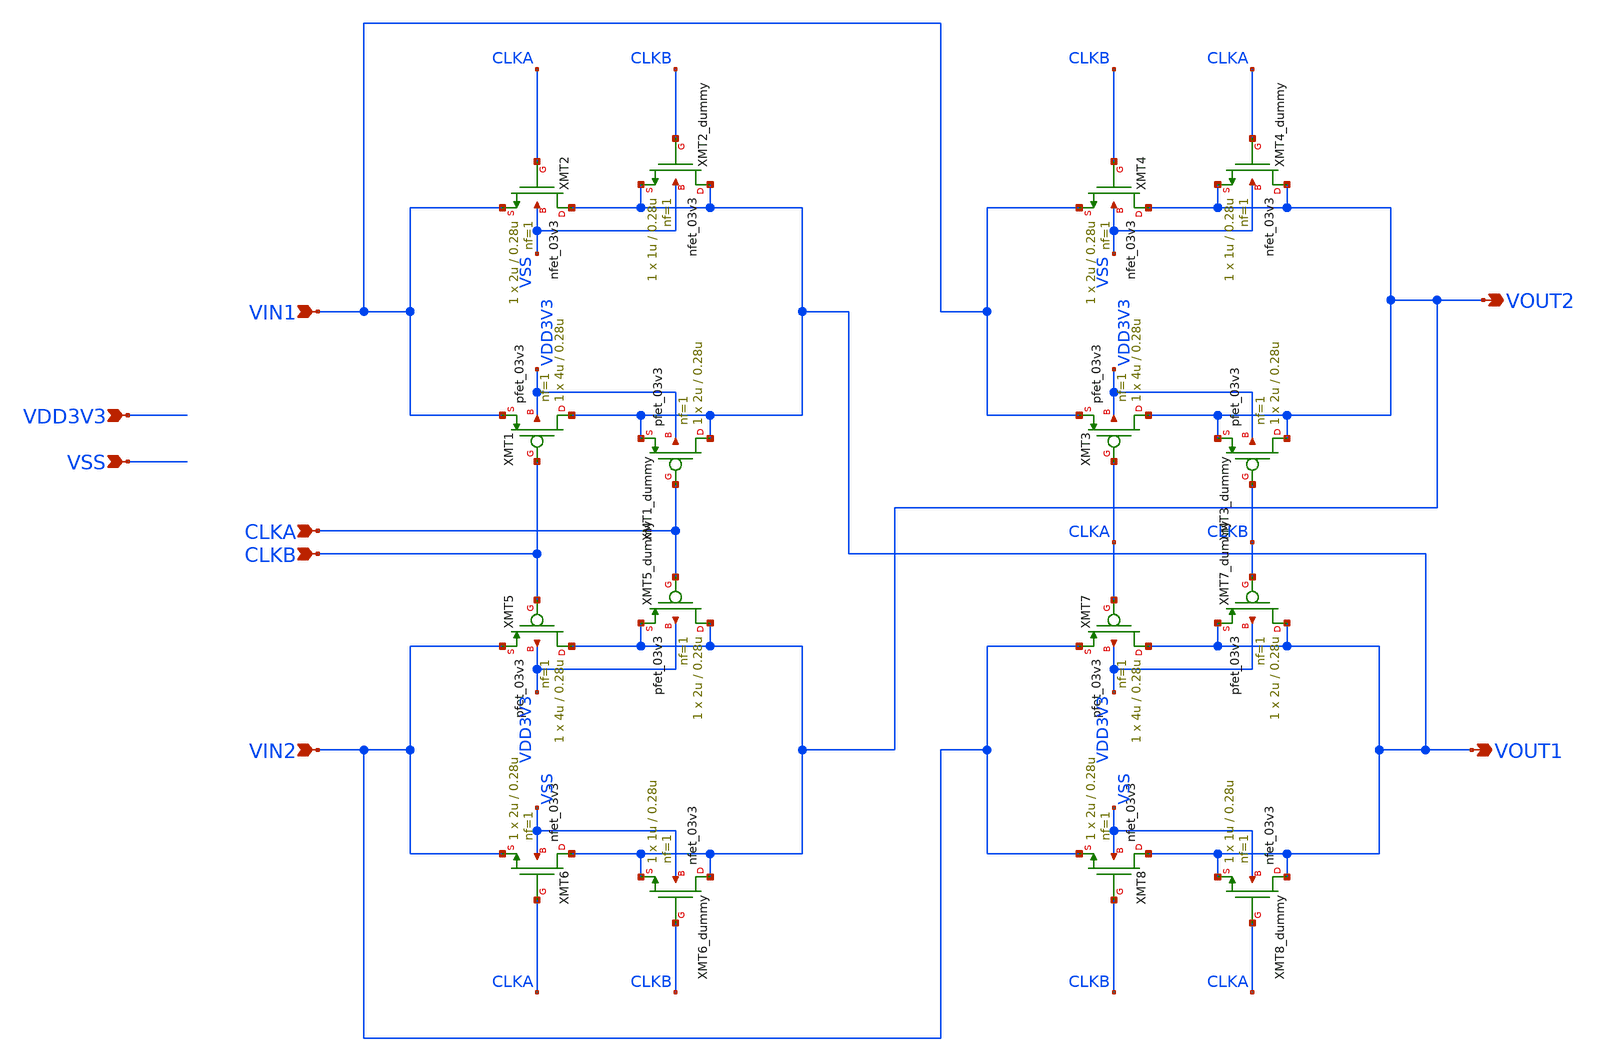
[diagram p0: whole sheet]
** sch_path: designs/libs/core_ina/ina_chopper/ina_chopper.sch
**.subckt ina_chopper VIN1 VIN2 CLKB VOUT2 CLKA VOUT1 VDD3V3 VSS
*.ipin VIN1
*.ipin VIN2
*.ipin CLKB
*.opin VOUT2
*.ipin CLKA
*.opin VOUT1
*.ipin VDD3V3
*.ipin VSS
XMT2 VOUT1 CLKA VIN1 VSS nfet_03v3 L=0.28u W=2u nf=1 ad='int((nf+1)/2) * W/nf * 0.18u' as='int((nf+2)/2) * W/nf * 0.18u'
+ pd='2*int((nf+1)/2) * (W/nf + 0.18u)' ps='2*int((nf+2)/2) * (W/nf + 0.18u)' nrd='0.18u / W' nrs='0.18u / W'
+ sa=0 sb=0 sd=0 m=1
XMT1 VOUT1 CLKB VIN1 VDD3V3 pfet_03v3 L=0.28u W=4u nf=1 ad='int((nf+1)/2) * W/nf * 0.18u' as='int((nf+2)/2) * W/nf * 0.18u'
+ pd='2*int((nf+1)/2) * (W/nf + 0.18u)' ps='2*int((nf+2)/2) * (W/nf + 0.18u)' nrd='0.18u / W' nrs='0.18u / W'
+ sa=0 sb=0 sd=0 m=1
XMT4 VOUT2 CLKB VIN1 VSS nfet_03v3 L=0.28u W=2u nf=1 ad='int((nf+1)/2) * W/nf * 0.18u' as='int((nf+2)/2) * W/nf * 0.18u'
+ pd='2*int((nf+1)/2) * (W/nf + 0.18u)' ps='2*int((nf+2)/2) * (W/nf + 0.18u)' nrd='0.18u / W' nrs='0.18u / W'
+ sa=0 sb=0 sd=0 m=1
XMT3 VOUT2 CLKA VIN1 VDD3V3 pfet_03v3 L=0.28u W=4u nf=1 ad='int((nf+1)/2) * W/nf * 0.18u' as='int((nf+2)/2) * W/nf * 0.18u'
+ pd='2*int((nf+1)/2) * (W/nf + 0.18u)' ps='2*int((nf+2)/2) * (W/nf + 0.18u)' nrd='0.18u / W' nrs='0.18u / W'
+ sa=0 sb=0 sd=0 m=1
XMT6 VOUT2 CLKA VIN2 VSS nfet_03v3 L=0.28u W=2u nf=1 ad='int((nf+1)/2) * W/nf * 0.18u' as='int((nf+2)/2) * W/nf * 0.18u'
+ pd='2*int((nf+1)/2) * (W/nf + 0.18u)' ps='2*int((nf+2)/2) * (W/nf + 0.18u)' nrd='0.18u / W' nrs='0.18u / W'
+ sa=0 sb=0 sd=0 m=1
XMT5 VOUT2 CLKB VIN2 VDD3V3 pfet_03v3 L=0.28u W=4u nf=1 ad='int((nf+1)/2) * W/nf * 0.18u' as='int((nf+2)/2) * W/nf * 0.18u'
+ pd='2*int((nf+1)/2) * (W/nf + 0.18u)' ps='2*int((nf+2)/2) * (W/nf + 0.18u)' nrd='0.18u / W' nrs='0.18u / W'
+ sa=0 sb=0 sd=0 m=1
XMT8 VOUT1 CLKB VIN2 VSS nfet_03v3 L=0.28u W=2u nf=1 ad='int((nf+1)/2) * W/nf * 0.18u' as='int((nf+2)/2) * W/nf * 0.18u'
+ pd='2*int((nf+1)/2) * (W/nf + 0.18u)' ps='2*int((nf+2)/2) * (W/nf + 0.18u)' nrd='0.18u / W' nrs='0.18u / W'
+ sa=0 sb=0 sd=0 m=1
XMT7 VOUT1 CLKA VIN2 VDD3V3 pfet_03v3 L=0.28u W=4u nf=1 ad='int((nf+1)/2) * W/nf * 0.18u' as='int((nf+2)/2) * W/nf * 0.18u'
+ pd='2*int((nf+1)/2) * (W/nf + 0.18u)' ps='2*int((nf+2)/2) * (W/nf + 0.18u)' nrd='0.18u / W' nrs='0.18u / W'
+ sa=0 sb=0 sd=0 m=1
XMT2_dummy VOUT1 CLKB VOUT1 VSS nfet_03v3 L=0.28u W=1u nf=1 ad='int((nf+1)/2) * W/nf * 0.18u' as='int((nf+2)/2) * W/nf * 0.18u'
+ pd='2*int((nf+1)/2) * (W/nf + 0.18u)' ps='2*int((nf+2)/2) * (W/nf + 0.18u)' nrd='0.18u / W' nrs='0.18u / W'
+ sa=0 sb=0 sd=0 m=1
XMT1_dummy VOUT1 CLKA VOUT1 VDD3V3 pfet_03v3 L=0.28u W=2u nf=1 ad='int((nf+1)/2) * W/nf * 0.18u' as='int((nf+2)/2) * W/nf * 0.18u'
+ pd='2*int((nf+1)/2) * (W/nf + 0.18u)' ps='2*int((nf+2)/2) * (W/nf + 0.18u)' nrd='0.18u / W' nrs='0.18u / W'
+ sa=0 sb=0 sd=0 m=1
XMT4_dummy VOUT2 CLKA VOUT2 VSS nfet_03v3 L=0.28u W=1u nf=1 ad='int((nf+1)/2) * W/nf * 0.18u' as='int((nf+2)/2) * W/nf * 0.18u'
+ pd='2*int((nf+1)/2) * (W/nf + 0.18u)' ps='2*int((nf+2)/2) * (W/nf + 0.18u)' nrd='0.18u / W' nrs='0.18u / W'
+ sa=0 sb=0 sd=0 m=1
XMT3_dummy VOUT2 CLKB VOUT2 VDD3V3 pfet_03v3 L=0.28u W=2u nf=1 ad='int((nf+1)/2) * W/nf * 0.18u' as='int((nf+2)/2) * W/nf * 0.18u'
+ pd='2*int((nf+1)/2) * (W/nf + 0.18u)' ps='2*int((nf+2)/2) * (W/nf + 0.18u)' nrd='0.18u / W' nrs='0.18u / W'
+ sa=0 sb=0 sd=0 m=1
XMT5_dummy VOUT2 CLKA VOUT2 VDD3V3 pfet_03v3 L=0.28u W=2u nf=1 ad='int((nf+1)/2) * W/nf * 0.18u' as='int((nf+2)/2) * W/nf * 0.18u'
+ pd='2*int((nf+1)/2) * (W/nf + 0.18u)' ps='2*int((nf+2)/2) * (W/nf + 0.18u)' nrd='0.18u / W' nrs='0.18u / W'
+ sa=0 sb=0 sd=0 m=1
XMT6_dummy VOUT2 CLKB VOUT2 VSS nfet_03v3 L=0.28u W=1u nf=1 ad='int((nf+1)/2) * W/nf * 0.18u' as='int((nf+2)/2) * W/nf * 0.18u'
+ pd='2*int((nf+1)/2) * (W/nf + 0.18u)' ps='2*int((nf+2)/2) * (W/nf + 0.18u)' nrd='0.18u / W' nrs='0.18u / W'
+ sa=0 sb=0 sd=0 m=1
XMT7_dummy VOUT1 CLKB VOUT1 VDD3V3 pfet_03v3 L=0.28u W=2u nf=1 ad='int((nf+1)/2) * W/nf * 0.18u' as='int((nf+2)/2) * W/nf * 0.18u'
+ pd='2*int((nf+1)/2) * (W/nf + 0.18u)' ps='2*int((nf+2)/2) * (W/nf + 0.18u)' nrd='0.18u / W' nrs='0.18u / W'
+ sa=0 sb=0 sd=0 m=1
XMT8_dummy VOUT1 CLKA VOUT1 VSS nfet_03v3 L=0.28u W=1u nf=1 ad='int((nf+1)/2) * W/nf * 0.18u' as='int((nf+2)/2) * W/nf * 0.18u'
+ pd='2*int((nf+1)/2) * (W/nf + 0.18u)' ps='2*int((nf+2)/2) * (W/nf + 0.18u)' nrd='0.18u / W' nrs='0.18u / W'
+ sa=0 sb=0 sd=0 m=1
**.ends
.end
